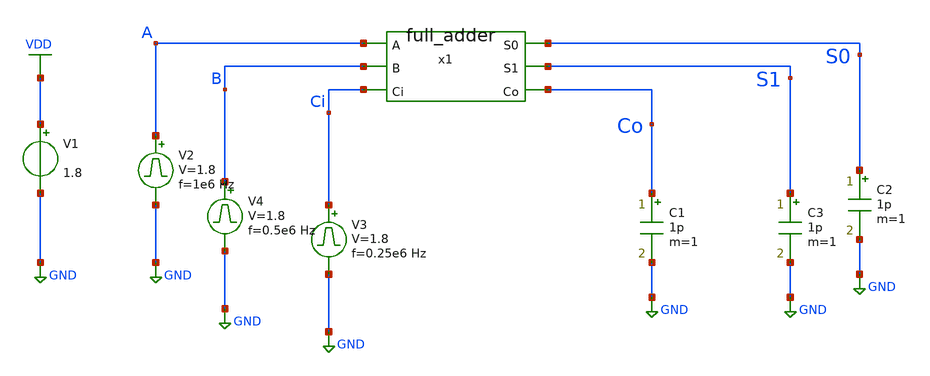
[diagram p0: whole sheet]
** sch_path: circuits/xschem/full_adder_tb.sch
**.subckt full_adder_tb
V1 VDD GND 1.8
V2 A GND pulse 0 1.8 '0.495/ 1e6 ' '0.01/1e6 ' '0.01/1e6 ' '0.49/1e6 ' '1/1e6 '
C1 Co GND 1p m=1
V3 Ci GND pulse 0 1.8 '0.495/ 0.25e6 ' '0.01/0.25e6 ' '0.01/0.25e6 ' '0.49/0.25e6 ' '1/0.25e6 '
C2 S0 GND 1p m=1
x1 A S0 B S1 Co Ci full_adder
C3 S1 GND 1p m=1
V4 B GND pulse 0 1.8 '0.495/ 0.5e6 ' '0.01/0.5e6 ' '0.01/0.5e6 ' '0.49/0.5e6 ' '1/0.5e6 '
**** begin user architecture code


.control
save all
tran 1n 4u
plot V(A) V(B)+2 V(Ci)+4 V(S0)+6 V(S1)+8 V(Co)+10
.endc



** opencircuitdesign pdks install
.lib $::SKYWATER_MODELS/sky130.lib.spice tt


**** end user architecture code
**.ends
.GLOBAL VDD
.GLOBAL GND
.end
